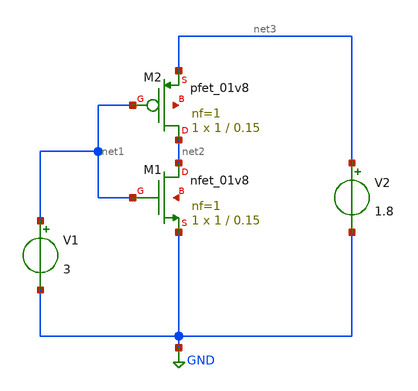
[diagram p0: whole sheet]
** sch_path: week0/inverter.sch
**.subckt inverter
XM1 net2 net1 GND net4 sky130_fd_pr__nfet_01v8 L=0.15 W=1 nf=1 ad='int((nf+1)/2) * W/nf * 0.29' as='int((nf+2)/2) * W/nf * 0.29'
+ pd='2*int((nf+1)/2) * (W/nf + 0.29)' ps='2*int((nf+2)/2) * (W/nf + 0.29)' nrd='0.29 / W' nrs='0.29 / W'
+ sa=0 sb=0 sd=0 mult=1 m=1
V1 net1 GND 3
V2 net3 GND 1.8
XM2 net2 net1 net3 net5 sky130_fd_pr__pfet_01v8 L=0.15 W=1 nf=1 ad='int((nf+1)/2) * W/nf * 0.29' as='int((nf+2)/2) * W/nf * 0.29'
+ pd='2*int((nf+1)/2) * (W/nf + 0.29)' ps='2*int((nf+2)/2) * (W/nf + 0.29)' nrd='0.29 / W' nrs='0.29 / W'
+ sa=0 sb=0 sd=0 mult=1 m=1
**** begin user architecture code



.lib ~/Downloads/open_pdks/sky130/sky130A/libs.tech/ngspice/sky130.lib.spice tt

.control
	.tran 0 0 3
	plot
.endc

.save all



**** end user architecture code
**.ends
.GLOBAL GND
.end
